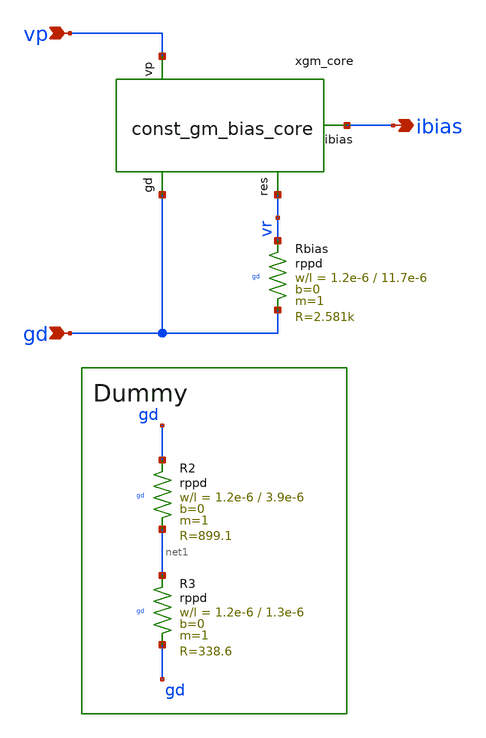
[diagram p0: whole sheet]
** sch_path: circuit/const_gm_bias.sch
**.subckt const_gm_bias ibias vp gd
*.opin ibias
*.ipin vp
*.ipin gd
xgm_core vp ibias gd vr const_gm_bias_core
XRbias vr gd gd rppd w=1.2e-6 l=11.7e-6 m=1 b=0 mm_ok=1
XR2 gd net1 gd rppd w=1.2e-6 l=3.9e-6 m=1 b=0 mm_ok=1
XR3 net1 gd gd rppd w=1.2e-6 l=1.3e-6 m=1 b=0 mm_ok=1
**.ends

* expanding   symbol:  /foss/designs/test/circuit/const_gm_bias_core.sym # of pins=4
** sym_path: circuit/const_gm_bias_core.sym
** sch_path: circuit/const_gm_bias_core.sch
.subckt const_gm_bias_core vp ibias gd res
*.ipin vp
*.ipin gd
*.opin ibias
*.opin res
XM1 net1 nbias gd gd sg13_hv_nmos w=0.6u l=2u ng=1 m=2 mm_ok=1
XM3 net2 nbias res gd sg13_hv_nmos w=0.6u l=2u ng=1 m=4 mm_ok=1
XM8 net5 pbias vp vp sg13_hv_pmos w=0.6u l=2u ng=1 m=2 mm_ok=1
XM6 net4 pbias vp vp sg13_hv_pmos w=0.6u l=2u ng=1 m=2 mm_ok=1
XM10 net3 pbias vp vp sg13_hv_pmos w=0.6u l=2u ng=1 m=2 mm_ok=1
XM13 net6 gd vp vp sg13_hv_pmos w=0.6u l=4.38u ng=1 m=1 mm_ok=1
XM11 stup nbias gd gd sg13_hv_nmos w=0.6u l=2u ng=1 m=4 mm_ok=1
XM800 pbias stup gd gd sg13_hv_nmos w=0.6u l=2u ng=1 m=2 mm_ok=1
XM2 nbias nbias net1 gd sg13_hv_nmos w=0.6u l=2u ng=1 m=2 mm_ok=1
XM4 pbias nbias net2 gd sg13_hv_nmos w=0.6u l=2u ng=1 m=4 mm_ok=1
XM9 ibias pbias net3 vp sg13_hv_pmos w=0.6u l=2u ng=1 m=2 mm_ok=1
XM7 pbias pbias net5 vp sg13_hv_pmos w=0.6u l=2u ng=1 m=2 mm_ok=1
XM5 nbias pbias net4 vp sg13_hv_pmos w=0.6u l=2u ng=1 m=2 mm_ok=1
XM12 stup gd net6 vp sg13_hv_pmos w=0.6u l=4.38u ng=1 m=1 mm_ok=1
.ends

.end
